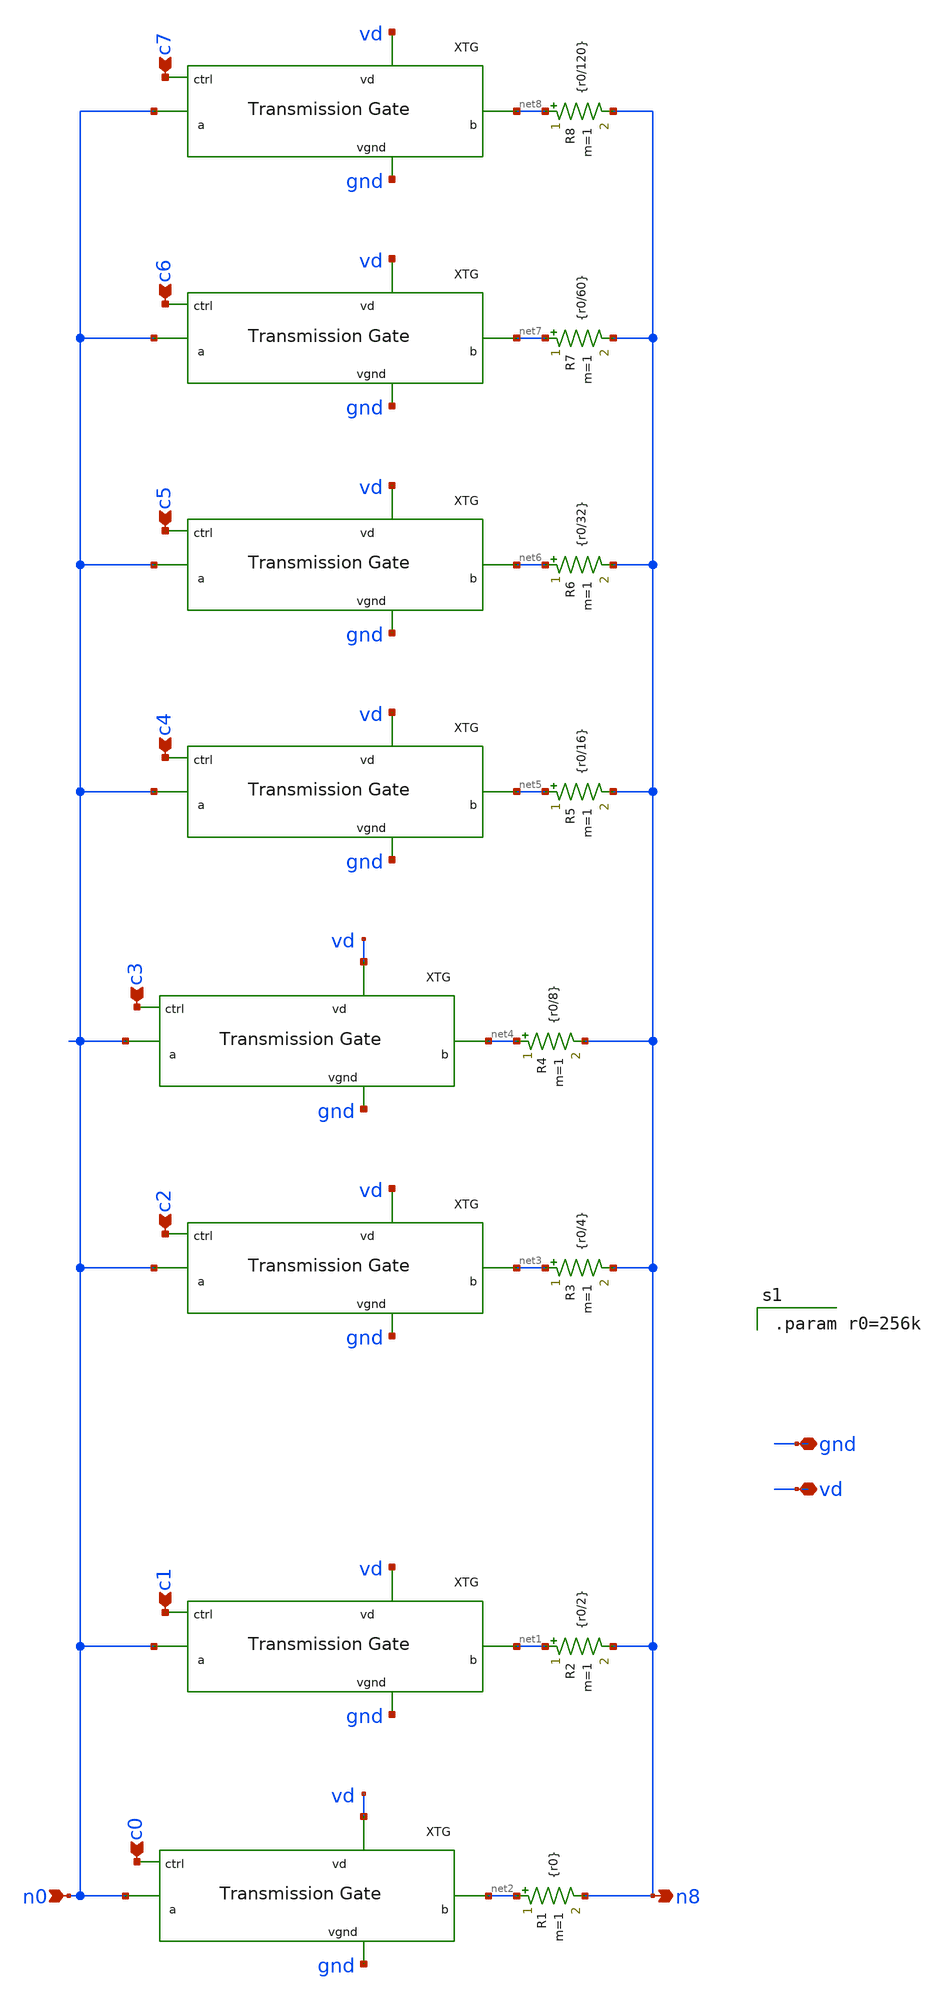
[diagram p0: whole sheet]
** sch_path: xschem/digpotp_r_ideal.sch
**.subckt digpotp_r_ideal gnd vd c0 c1 n0 n8 c2 c3 c4 c5 c6 c7
*.iopin gnd
*.iopin vd
*.ipin c0
*.ipin c1
*.ipin n0
*.opin n8
*.ipin c2
*.ipin c3
*.ipin c4
*.ipin c5
*.ipin c6
*.ipin c7
x9 c0 vd net2 gnd n0 tg
x10 c1 vd net1 gnd n0 tg
x7 c2 vd net3 gnd n0 tg
x8 c3 vd net4 gnd n0 tg
x11 c4 vd net5 gnd n0 tg
x12 c5 vd net6 gnd n0 tg
x1 c6 vd net7 gnd n0 tg
x2 c7 vd net8 gnd n0 tg
R1 net2 n8 {r0} m=1
R2 net1 n8 {r0/2} m=1
R3 net3 n8 {r0/4} m=1
R4 net4 n8 {r0/8} m=1
R5 net5 n8 {r0/16} m=1
R6 net6 n8 {r0/32} m=1
R7 net7 n8 {r0/60} m=1
R8 net8 n8 {r0/120} m=1
**** begin user architecture code

.param r0=256k

**** end user architecture code
**.ends

* expanding   symbol:  projects/dpga-ieee-sscs-contest/xschem/tg.sym # of pins=5
** sym_path: projects/dpga-ieee-sscs-contest/xschem/tg.sym
** sch_path: projects/dpga-ieee-sscs-contest/xschem/tg.sch
.subckt tg ctrl vd b vgnd a
*.iopin vd
*.iopin vgnd
*.iopin b
*.iopin a
*.ipin ctrl
XM2 b nctrl a vd sky130_fd_pr__pfet_01v8 L=0.15 W=60 nf=12 ad='int((nf+1)/2) * W/nf * 0.29' as='int((nf+2)/2) * W/nf * 0.29'
+ pd='2*int((nf+1)/2) * (W/nf + 0.29)' ps='2*int((nf+2)/2) * (W/nf + 0.29)' nrd='0.29 / W' nrs='0.29 / W'
+ sa=0 sb=0 sd=0 mult=1 m=1
XM1 a ctrl b vgnd sky130_fd_pr__nfet_01v8 L=0.15 W=60 nf=12 ad='int((nf+1)/2) * W/nf * 0.29' as='int((nf+2)/2) * W/nf * 0.29'
+ pd='2*int((nf+1)/2) * (W/nf + 0.29)' ps='2*int((nf+2)/2) * (W/nf + 0.29)' nrd='0.29 / W' nrs='0.29 / W'
+ sa=0 sb=0 sd=0 mult=1 m=1
XM3 nctrl ctrl vgnd vgnd sky130_fd_pr__nfet_01v8 L=0.15 W=1 nf=1 ad='int((nf+1)/2) * W/nf * 0.29' as='int((nf+2)/2) * W/nf * 0.29'
+ pd='2*int((nf+1)/2) * (W/nf + 0.29)' ps='2*int((nf+2)/2) * (W/nf + 0.29)' nrd='0.29 / W' nrs='0.29 / W'
+ sa=0 sb=0 sd=0 mult=1 m=1
XM4 nctrl ctrl vd vd sky130_fd_pr__pfet_01v8 L=0.15 W=3 nf=1 ad='int((nf+1)/2) * W/nf * 0.29' as='int((nf+2)/2) * W/nf * 0.29'
+ pd='2*int((nf+1)/2) * (W/nf + 0.29)' ps='2*int((nf+2)/2) * (W/nf + 0.29)' nrd='0.29 / W' nrs='0.29 / W'
+ sa=0 sb=0 sd=0 mult=1 m=1
.ends

.end
